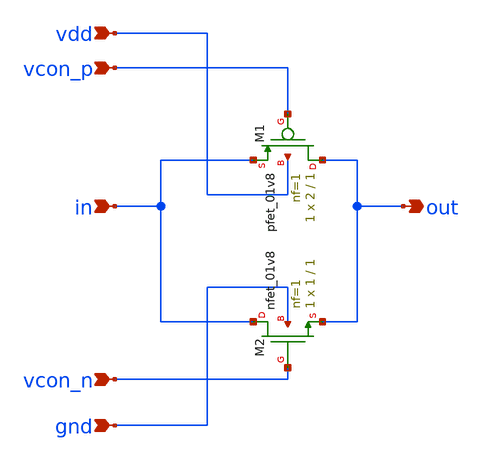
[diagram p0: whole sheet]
** sch_path: xschem/tg.sch
**.subckt tg vcon_p vdd vcon_n gnd in out
*.ipin vcon_p
*.ipin vdd
*.ipin vcon_n
*.ipin gnd
*.ipin in
*.opin out
XM1 out vcon_p in vdd sky130_fd_pr__pfet_01v8 L=1 W=2 nf=1 ad='int((nf+1)/2) * W/nf * 0.29' as='int((nf+2)/2) * W/nf * 0.29'
+ pd='2*int((nf+1)/2) * (W/nf + 0.29)' ps='2*int((nf+2)/2) * (W/nf + 0.29)' nrd='0.29 / W' nrs='0.29 / W'
+ sa=0 sb=0 sd=0 mult=1 m=1
XM2 in vcon_n out gnd sky130_fd_pr__nfet_01v8 L=1 W=1 nf=1 ad='int((nf+1)/2) * W/nf * 0.29' as='int((nf+2)/2) * W/nf * 0.29'
+ pd='2*int((nf+1)/2) * (W/nf + 0.29)' ps='2*int((nf+2)/2) * (W/nf + 0.29)' nrd='0.29 / W' nrs='0.29 / W'
+ sa=0 sb=0 sd=0 mult=1 m=1
**.ends
.end
